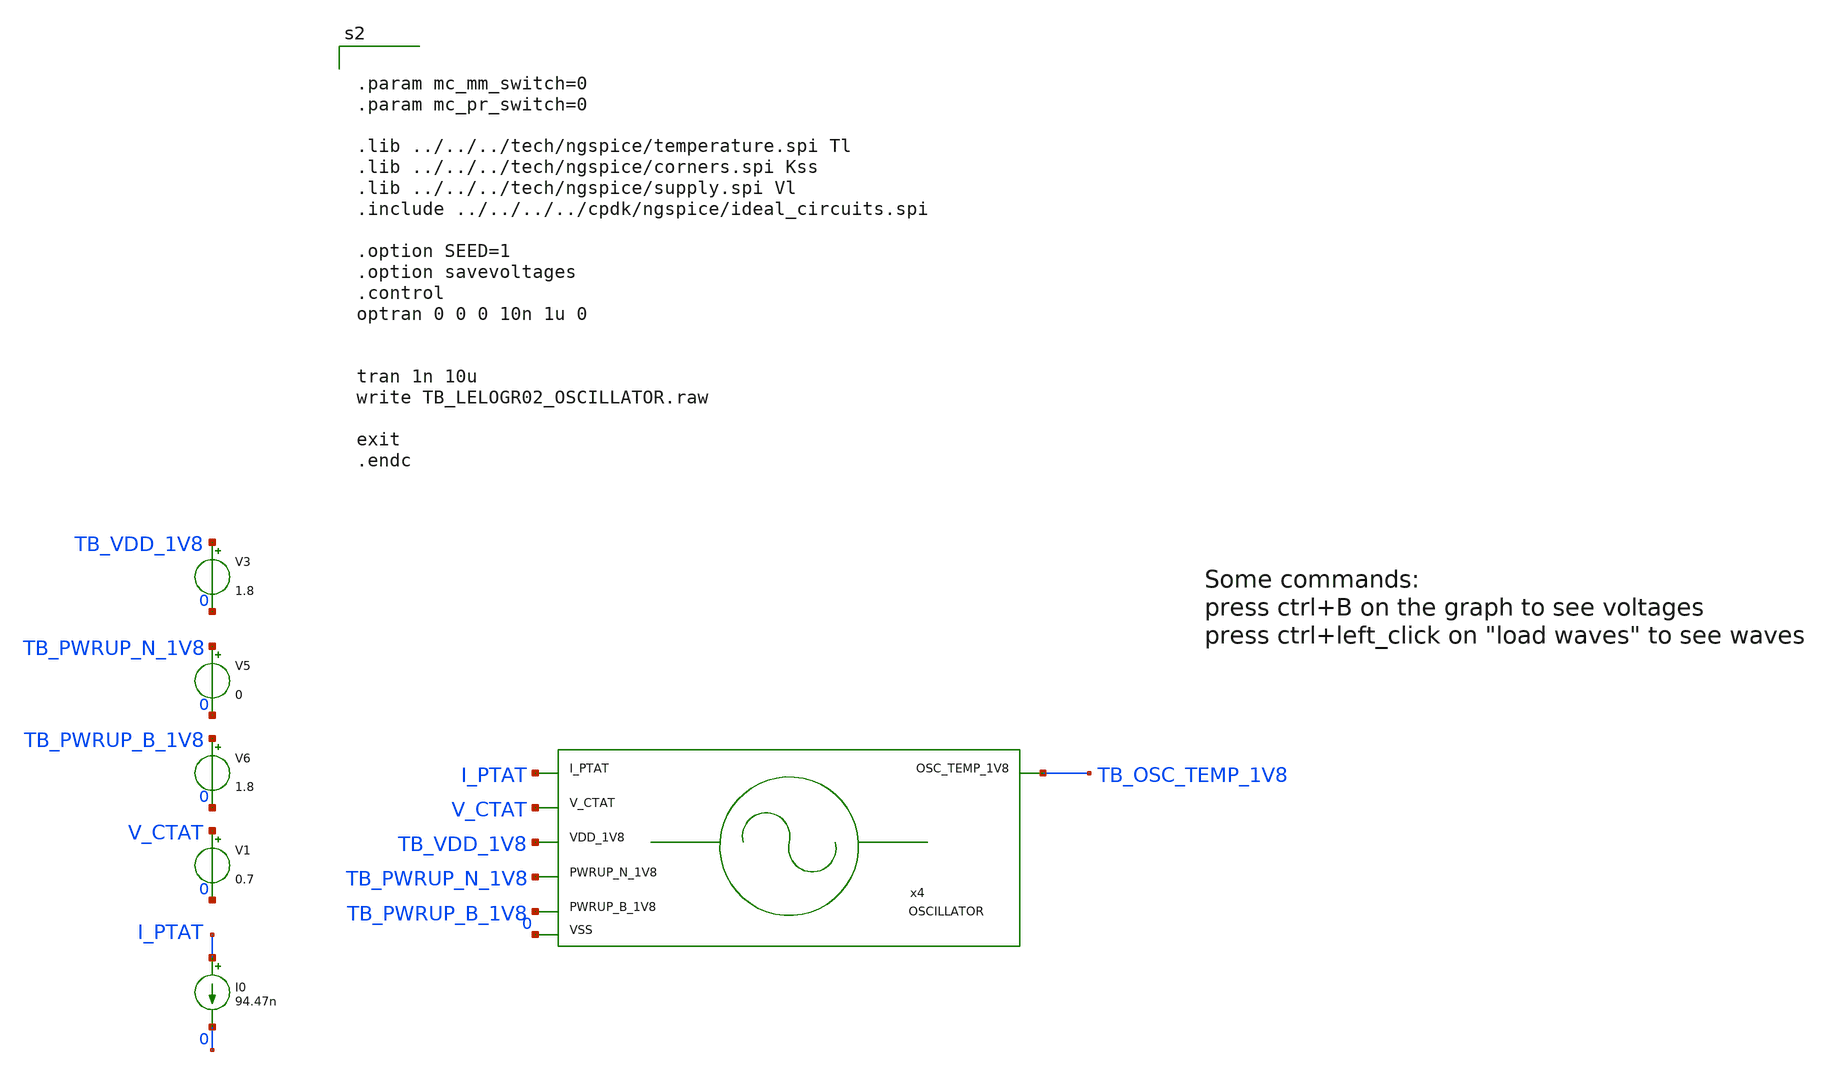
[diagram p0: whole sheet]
** sch_path: design/LELO_GR02_SKY130A/TB_LELOGR02_OSCILLATOR.sch
**.subckt TB_LELOGR02_OSCILLATOR
x4 TB_OSC_TEMP_1V8 TB_VDD_1V8 TB_PWRUP_N_1V8 0 V_CTAT I_PTAT TB_PWRUP_B_1V8 OSCILLATOR
V5 TB_PWRUP_N_1V8 0 0
V6 TB_PWRUP_B_1V8 0 1.8
V1 V_CTAT 0 0.7
I0 I_PTAT 0 94.47n
V3 TB_VDD_1V8 0 1.8
**** begin user architecture code


.param mc_mm_switch=0
.param mc_pr_switch=0

.lib ../../../tech/ngspice/temperature.spi Tl
.lib ../../../tech/ngspice/corners.spi Kss
.lib ../../../tech/ngspice/supply.spi Vl
.include ../../../../cpdk/ngspice/ideal_circuits.spi

.option SEED=1
.option savevoltages
.control
optran 0 0 0 10n 1u 0


tran 1n 10u
write TB_LELOGR02_OSCILLATOR.raw

exit
.endc



**** end user architecture code
**.ends
.end
